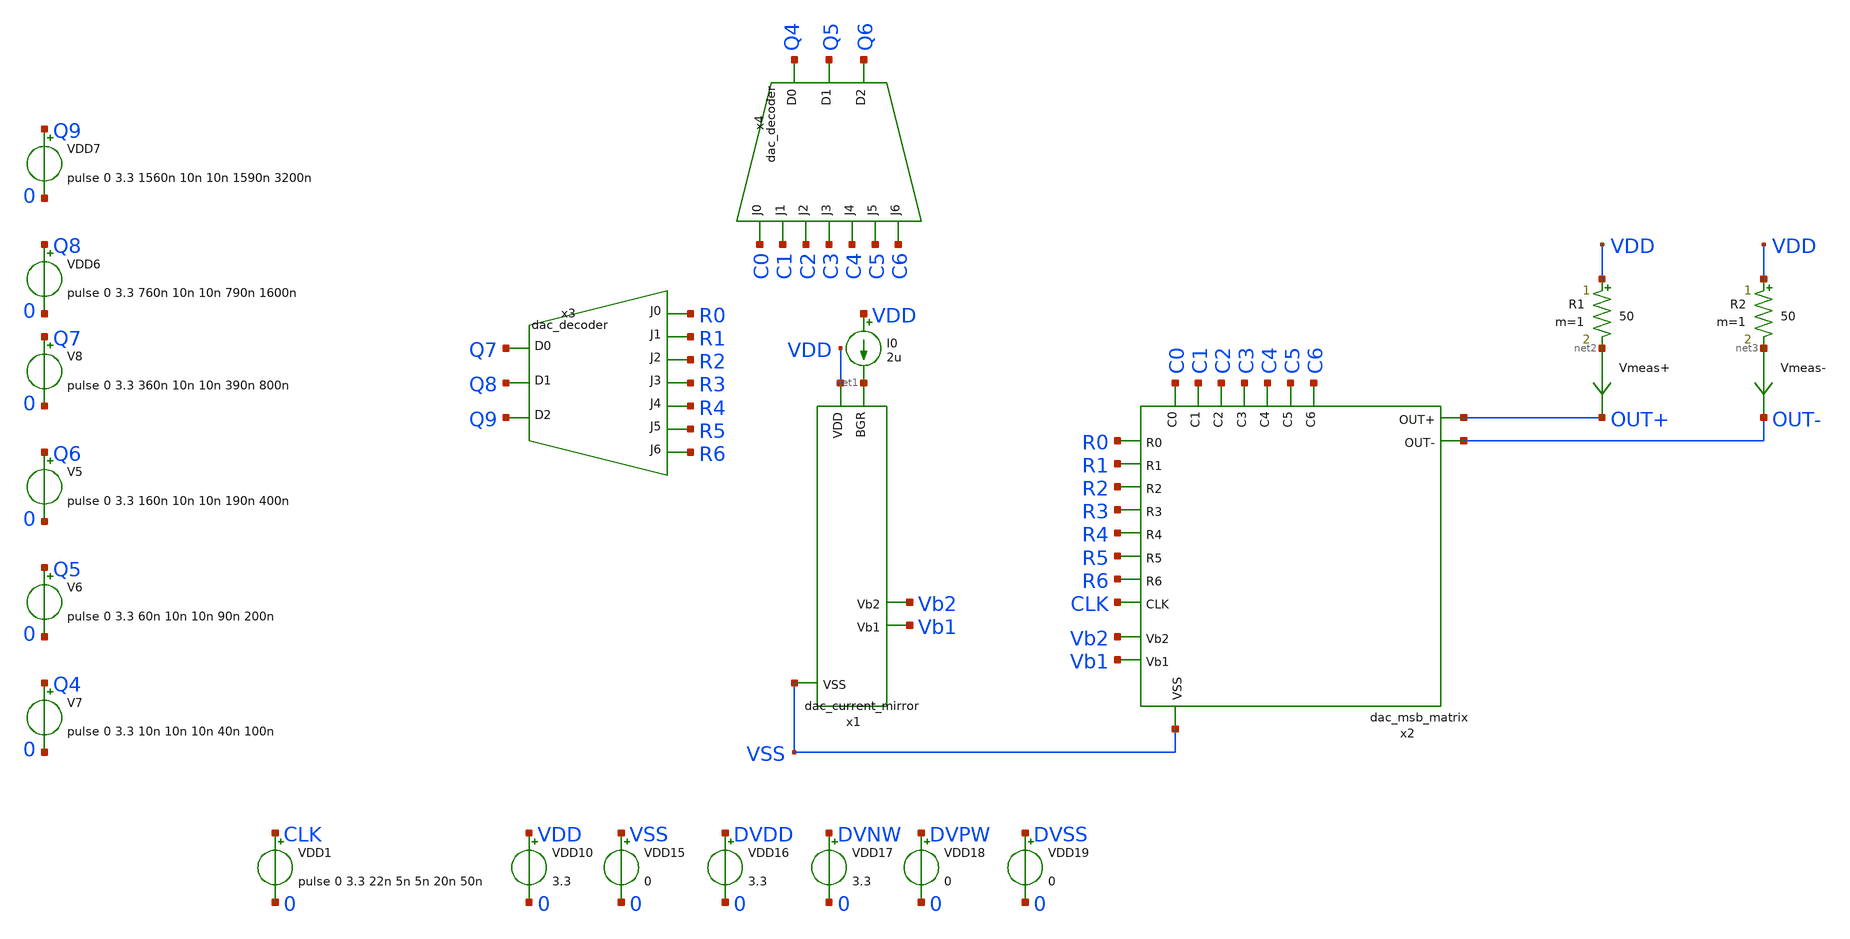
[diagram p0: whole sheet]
** sch_path: DAC/xschem/test_dac_msb_matrix.sch
**.subckt test_dac_msb_matrix
VDD6 Q8 0 pulse 0 3.3 760n 10n 10n 790n 1600n
VDD7 Q9 0 pulse 0 3.3 1560n 10n 10n 1590n 3200n
VDD10 VDD 0 3.3
VDD15 VSS 0 0
VDD16 DVDD 0 3.3
VDD17 DVNW 0 3.3
VDD18 DVPW 0 0
VDD19 DVSS 0 0
I0 VDD net1 2u
R1 VDD net2 50 m=1
R2 VDD net3 50 m=1
Vmeas+ net2 OUT+ 0
.save i(vmeas+)
Vmeas- net3 OUT- 0
.save i(vmeas-)
x1 VDD net1 Vb2 Vb1 VSS dac_current_mirror
x3 R6 R5 R4 R3 R2 R1 Q9 Q8 Q7 R0 VDD VNW VPW VSS dac_decoder
x4 C6 C5 C4 C3 C2 C1 Q6 Q5 Q4 C0 VDD VNW VPW VSS dac_decoder
V5 Q6 0 pulse 0 3.3 160n 10n 10n 190n 400n
V6 Q5 0 pulse 0 3.3 60n 10n 10n 90n 200n
V7 Q4 0 pulse 0 3.3 10n 10n 10n 40n 100n
V8 Q7 0 pulse 0 3.3 360n 10n 10n 390n 800n
VDD1 CLK 0 pulse 0 3.3 22n 5n 5n 20n 50n
x2 C5 C1 C4 C3 C2 C0 C6 R0 CLK OUT+ OUT- Vb2 Vb1 R1 R2 R3 R4 R5 R6 VSS DVDD DVNW DVPW DVSS
+ dac_msb_matrix
**** begin user architecture code




.control
	tran 1n 3200n
	plot i(Vmeas+) i(Vmeas-)
	write test_dac_msb_matrix.raw
.endc
.save all





.include $::180MCU_MODELS/design.ngspice
.lib $::180MCU_MODELS/sm141064.ngspice typical
.lib $::180MCU_MODELS/sm141064.ngspice res_typical
.lib $::180MCU_MODELS/sm141064.ngspice moscap_typical
.include $::180MCU_STDCELLS/spice/gf180mcu_fd_sc_mcu7t5v0.spice
*.lib $::180MCU_MODELS/sm141064.ngspice res_statistical

**** end user architecture code
**.ends
.end
